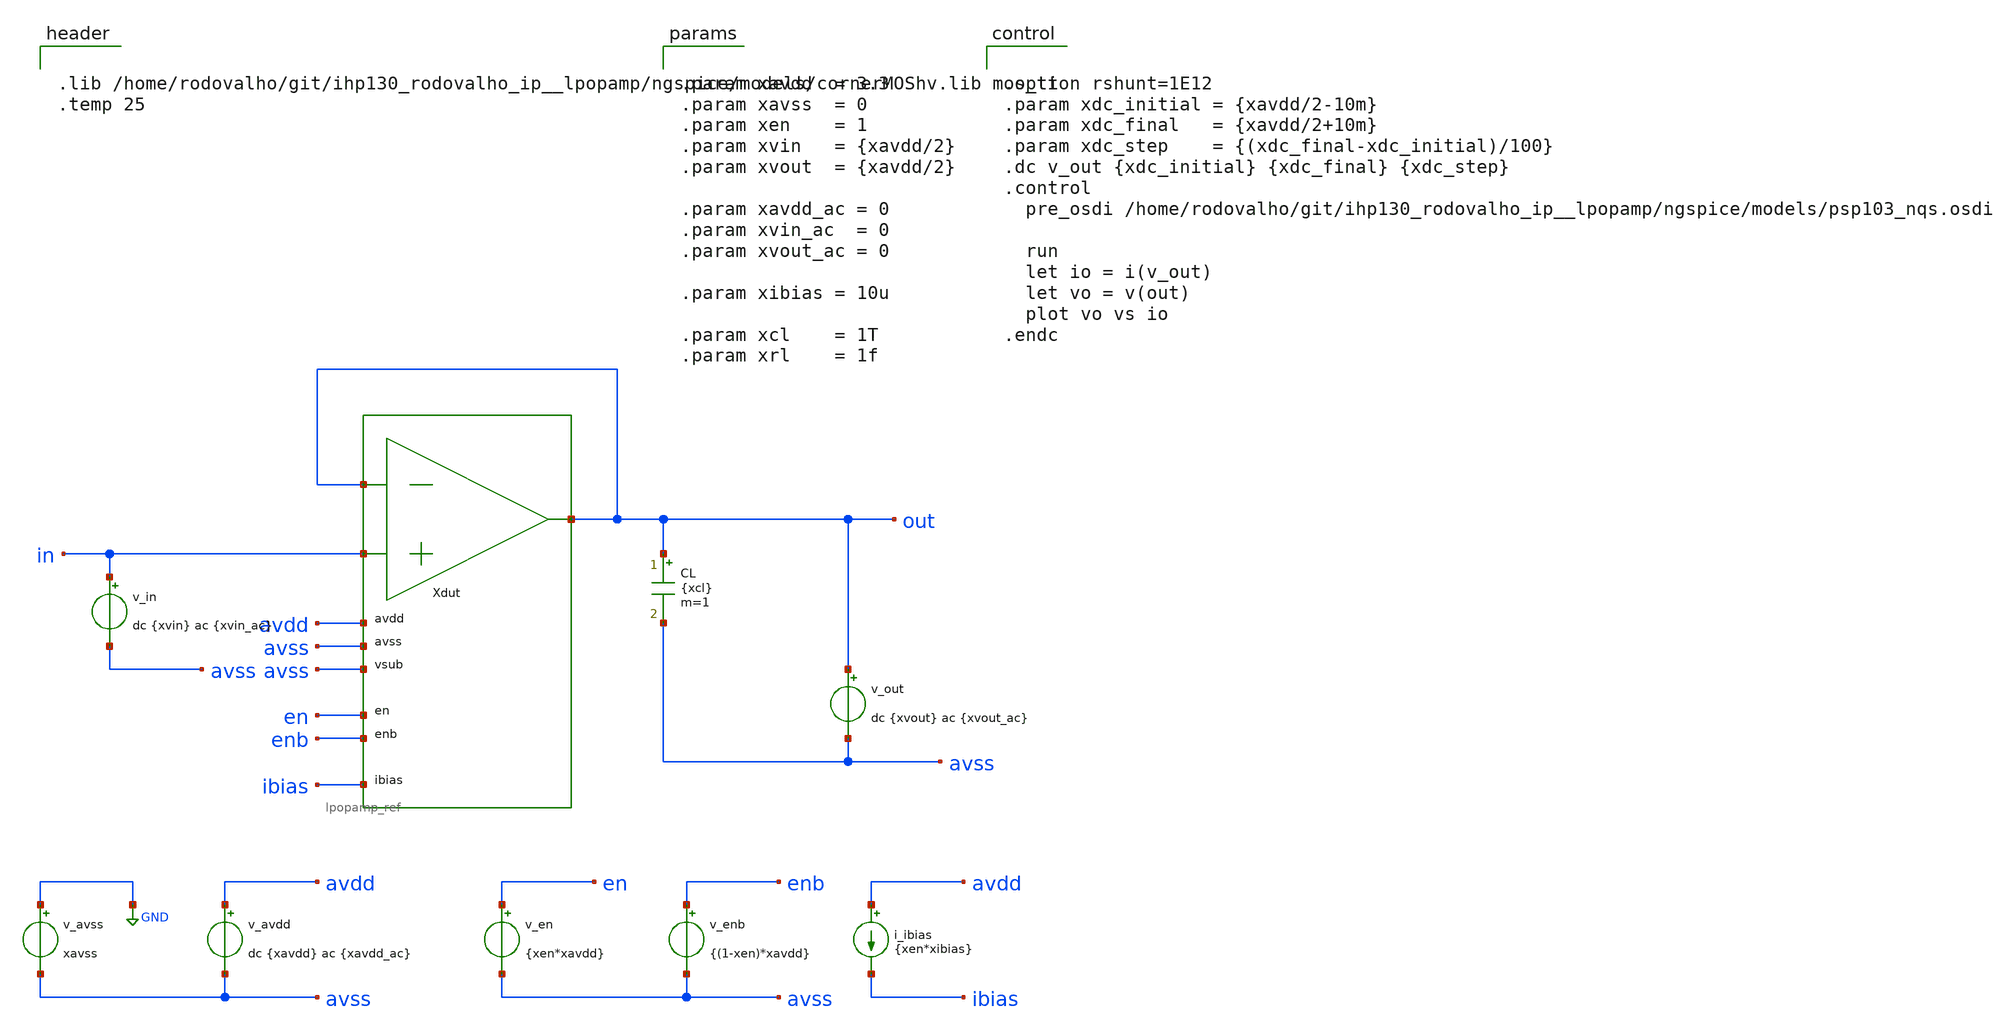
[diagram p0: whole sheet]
** sch_path: xschem/tb_lpopamp_buf_io.sch
**.subckt tb_lpopamp_buf_io
Xdut out in out avdd avss avss en enb ibias lpopamp_ref
v_avss GND avss xavss
v_avdd avdd avss dc {xavdd} ac {xavdd_ac}
v_in in avss dc {xvin} ac {xvin_ac}
v_en en avss {xen*xavdd}
v_enb enb avss {(1-xen)*xavdd}
i_ibias avdd ibias {xen*xibias}
CL out avss {xcl} m=1
v_out out avss dc {xvout} ac {xvout_ac}
**** begin user architecture code


.lib /home/rodovalho/git/ihp130_rodovalho_ip__lpopamp/ngspice/models/cornerMOShv.lib mos_tt
.temp 25




.option rshunt=1E12
.param xdc_initial = {xavdd/2-10m}
.param xdc_final   = {xavdd/2+10m}
.param xdc_step    = {(xdc_final-xdc_initial)/100}
.dc v_out {xdc_initial} {xdc_final} {xdc_step}
.control
  pre_osdi /home/rodovalho/git/ihp130_rodovalho_ip__lpopamp/ngspice/models/psp103_nqs.osdi

  run
  let io = i(v_out)
  let vo = v(out)
  plot vo vs io
.endc




.param xavdd  = 3.3
.param xavss  = 0
.param xen    = 1
.param xvin   = {xavdd/2}
.param xvout  = {xavdd/2}

.param xavdd_ac = 0
.param xvin_ac  = 0
.param xvout_ac = 0

.param xibias = 10u

.param xcl    = 1T
.param xrl    = 1f


**** end user architecture code
**.ends
.GLOBAL GND
.end
